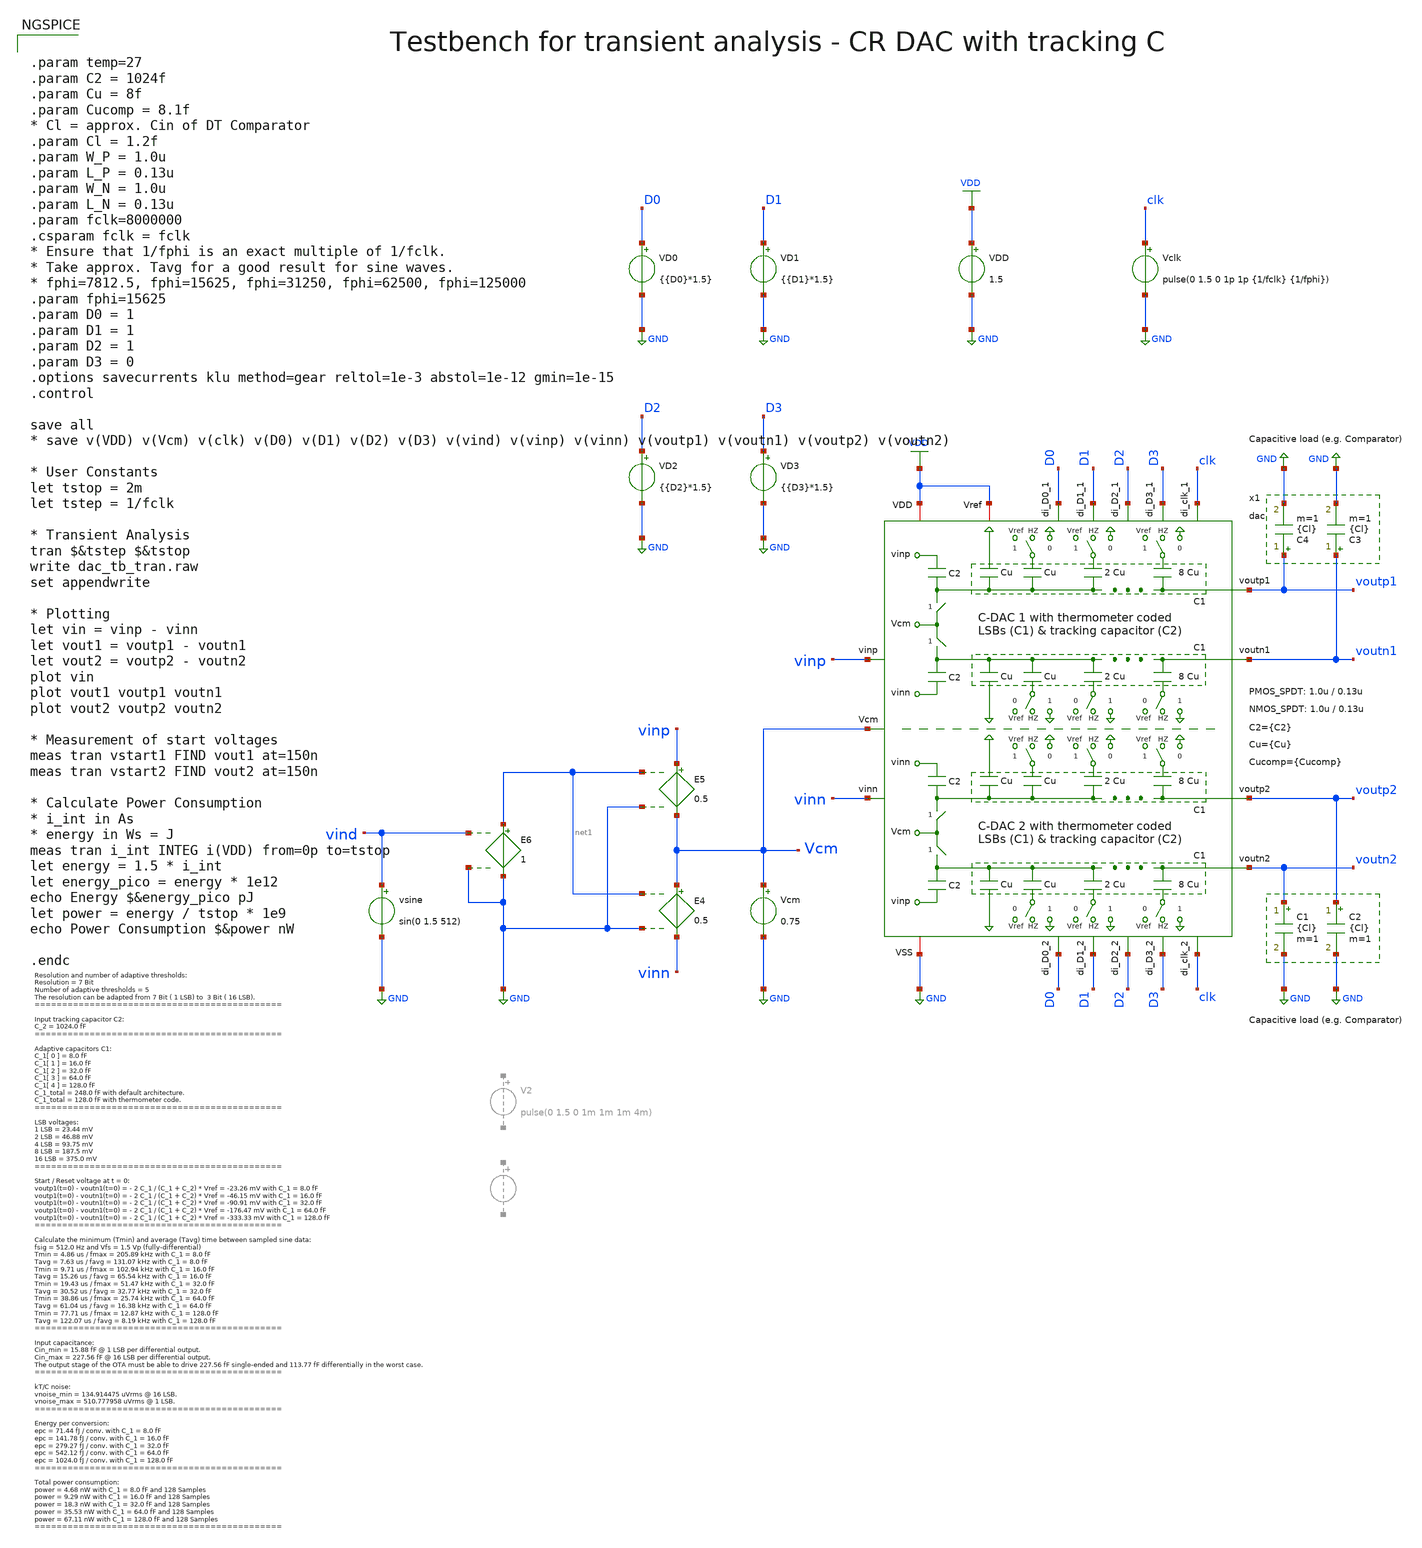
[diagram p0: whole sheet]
** sch_path: SG13G2_ATBS-ADC-main/xschem/dac/testbenches/dac_tb_tran.sch
**.subckt dac_tb_tran
VDD VDD GND 1.5
Vclk clk GND pulse(0 1.5 0 1p 1p {1/fclk} {1/fphi})
Vcm Vcm GND 0.75
E4 Vcm vinn net1 GND 0.5
E5 vinp Vcm net1 GND 0.5
E6 net1 GND vind GND 1
vsine vind GND sin(0 1.5 512)
VD0 D0 GND {{D0}*1.5}
VD1 D1 GND {{D1}*1.5}
VD2 D2 GND {{D2}*1.5}
VD3 D3 GND {{D3}*1.5}
C1 voutn2 GND {Cl} m=1
C2 voutp2 GND {Cl} m=1
C3 voutn1 GND {Cl} m=1
C4 voutp1 GND {Cl} m=1
x1 VDD vinp voutp1 voutn1 vinn D0 D1 D2 D3 GND VDD Vcm voutp2 voutn2 clk D0 D1 D2 D3 clk dac W_P_SPDT=1.0u
+ L_P_SPDT=0.13u W_N_SPDT=1.0u L_N_SPDT=0.13u C2={C2} Cu={Cu} Cucomp={Cucomp}
**** begin user architecture code

.lib cornerMOSlv.lib mos_tt
.lib cornerMOShv.lib mos_tt
.lib cornerRES.lib res_typ



.param temp=27
.param C2 = 1024f
.param Cu = 8f
.param Cucomp = 8.1f
* Cl = approx. Cin of DT Comparator
.param Cl = 1.2f
.param W_P = 1.0u
.param L_P = 0.13u
.param W_N = 1.0u
.param L_N = 0.13u
.param fclk=8000000
.csparam fclk = fclk
* Ensure that 1/fphi is an exact multiple of 1/fclk.
* Take approx. Tavg for a good result for sine waves.
* fphi=7812.5, fphi=15625, fphi=31250, fphi=62500, fphi=125000
.param fphi=15625
.param D0 = 1
.param D1 = 1
.param D2 = 1
.param D3 = 0
.options savecurrents klu method=gear reltol=1e-3 abstol=1e-12 gmin=1e-15
.control

save all
* save v(VDD) v(Vcm) v(clk) v(D0) v(D1) v(D2) v(D3) v(vind) v(vinp) v(vinn) v(voutp1) v(voutn1)
*+ v(voutp2) v(voutn2)

* User Constants
let tstop = 2m
let tstep = 1/fclk

* Transient Analysis
tran $&tstep $&tstop
write dac_tb_tran.raw
set appendwrite

* Plotting
let vin = vinp - vinn
let vout1 = voutp1 - voutn1
let vout2 = voutp2 - voutn2
plot vin
plot vout1 voutp1 voutn1
plot vout2 voutp2 voutn2

* Measurement of start voltages
meas tran vstart1 FIND vout1 at=150n
meas tran vstart2 FIND vout2 at=150n

* Calculate Power Consumption
* i_int in As
* energy in Ws = J
meas tran i_int INTEG i(VDD) from=0p to=tstop
let energy = 1.5 * i_int
let energy_pico = energy * 1e12
echo Energy $&energy_pico pJ
let power = energy / tstop * 1e9
echo Power Consumption $&power nW

.endc


**** end user architecture code
**.ends

* expanding   symbol:  dac/dac.sym # of pins=20
** sym_path: SG13G2_ATBS-ADC-main/xschem/dac/dac.sym
** sch_path: SG13G2_ATBS-ADC-main/xschem/dac/dac.sch
.subckt dac VDD vinp voutp1 voutn1 vinn di_D0_2 di_D1_2 di_D2_2 di_D3_2 VSS Vref Vcm voutp2 voutn2
+ di_clk_2 di_D0_1 di_D1_1 di_D2_1 di_D3_1 di_clk_1  W_P_SPDT=1.0u L_P_SPDT=0.13u W_N_SPDT=1.0u L_N_SPDT=0.13u
+ C2=1024f Cu=8f Cucomp=8.1f
*.opin voutp1
*.ipin di_D0_1
*.iopin VSS
*.iopin Vref
*.opin voutn1
*.ipin vinp
*.ipin vinn
*.ipin di_D1_1
*.ipin di_D2_1
*.ipin di_D3_1
*.opin voutp2
*.opin voutn2
*.iopin VDD
*.ipin Vcm
*.ipin di_clk_1
*.ipin di_D3_2
*.ipin di_D2_2
*.ipin di_D1_2
*.ipin di_D0_2
*.ipin di_clk_2
C2a vinp voutp1 C2 m=1
C2b vinn voutn1 C2 m=1
C1a net3 voutp1 Cucomp m=1
C1b net1 voutn1 Cucomp m=1
x2 VDD di_clk_1 VSS voutp1 Vcm clk_1_n transmission_gate_lv_wo_dummy W_P=1.0u L_P=0.13u W_N=1.0u
+ L_N=0.13u
x3 VDD di_clk_1 VSS voutn1 Vcm clk_1_n transmission_gate_lv_wo_dummy W_P=1.0u L_P=0.13u W_N=1.0u
+ L_N=0.13u
x1 VDD di_clk_1 clk_1_n VSS inverter_lv W_P=W_P_SPDT L_P=L_P_SPDT W_N=W_N_SPDT L_N=L_N_SPDT
x5 Vref VSS VSS di_D1_1 di_clk_1 VDD voutp1 unit_cell W_P_SPDT=W_P_SPDT L_P_SPDT=L_P_SPDT
+ W_N_SPDT=W_N_SPDT L_N_SPDT=L_N_SPDT Cu=2*Cu
x6 Vref VSS VSS di_D2_1 di_clk_1 VDD voutp1 unit_cell W_P_SPDT=W_P_SPDT L_P_SPDT=L_P_SPDT
+ W_N_SPDT=W_N_SPDT L_N_SPDT=L_N_SPDT Cu=4*Cu
x4 Vref VSS VSS di_D0_1 di_clk_1 VDD voutp1 unit_cell W_P_SPDT=W_P_SPDT L_P_SPDT=L_P_SPDT
+ W_N_SPDT=W_N_SPDT L_N_SPDT=L_N_SPDT Cu=Cu
x7 Vref VSS VSS di_D3_1 di_clk_1 VDD voutp1 unit_cell W_P_SPDT=W_P_SPDT L_P_SPDT=L_P_SPDT
+ W_N_SPDT=W_N_SPDT L_N_SPDT=L_N_SPDT Cu=8*Cu
x9 VSS Vref VSS di_D0_1 di_clk_1 VDD voutn1 unit_cell W_P_SPDT=W_P_SPDT L_P_SPDT=L_P_SPDT
+ W_N_SPDT=W_N_SPDT L_N_SPDT=L_N_SPDT Cu=Cu
x10 VSS Vref VSS di_D1_1 di_clk_1 VDD voutn1 unit_cell W_P_SPDT=W_P_SPDT L_P_SPDT=L_P_SPDT
+ W_N_SPDT=W_N_SPDT L_N_SPDT=L_N_SPDT Cu=2*Cu
x11 VSS Vref VSS di_D2_1 di_clk_1 VDD voutn1 unit_cell W_P_SPDT=W_P_SPDT L_P_SPDT=L_P_SPDT
+ W_N_SPDT=W_N_SPDT L_N_SPDT=L_N_SPDT Cu=4*Cu
x12 VSS Vref VSS di_D3_1 di_clk_1 VDD voutn1 unit_cell W_P_SPDT=W_P_SPDT L_P_SPDT=L_P_SPDT
+ W_N_SPDT=W_N_SPDT L_N_SPDT=L_N_SPDT Cu=8*Cu
C1 vinn voutp2 C2 m=1
C2 vinp voutn2 C2 m=1
C1c net2 voutp2 Cucomp m=1
C1d net4 voutn2 Cucomp m=1
x14 VDD di_clk_2 VSS voutp2 Vcm clk_2_n transmission_gate_lv_wo_dummy W_P=1.0u L_P=0.13u W_N=1.0u
+ L_N=0.13u
x15 VDD di_clk_2 VSS voutn2 Vcm clk_2_n transmission_gate_lv_wo_dummy W_P=1.0u L_P=0.13u W_N=1.0u
+ L_N=0.13u
x17 Vref VSS VSS di_D1_2 di_clk_2 VDD voutp2 unit_cell W_P_SPDT=W_P_SPDT L_P_SPDT=L_P_SPDT
+ W_N_SPDT=W_N_SPDT L_N_SPDT=L_N_SPDT Cu=2*Cu
x18 Vref VSS VSS di_D2_2 di_clk_2 VDD voutp2 unit_cell W_P_SPDT=W_P_SPDT L_P_SPDT=L_P_SPDT
+ W_N_SPDT=W_N_SPDT L_N_SPDT=L_N_SPDT Cu=4*Cu
x16 Vref VSS VSS di_D0_2 di_clk_2 VDD voutp2 unit_cell W_P_SPDT=W_P_SPDT L_P_SPDT=L_P_SPDT
+ W_N_SPDT=W_N_SPDT L_N_SPDT=L_N_SPDT Cu=Cu
x19 Vref VSS VSS di_D3_2 di_clk_2 VDD voutp2 unit_cell W_P_SPDT=W_P_SPDT L_P_SPDT=L_P_SPDT
+ W_N_SPDT=W_N_SPDT L_N_SPDT=L_N_SPDT Cu=8*Cu
x21 VSS Vref VSS di_D0_2 di_clk_2 VDD voutn2 unit_cell W_P_SPDT=W_P_SPDT L_P_SPDT=L_P_SPDT
+ W_N_SPDT=W_N_SPDT L_N_SPDT=L_N_SPDT Cu=Cu
x22 VSS Vref VSS di_D1_2 di_clk_2 VDD voutn2 unit_cell W_P_SPDT=W_P_SPDT L_P_SPDT=L_P_SPDT
+ W_N_SPDT=W_N_SPDT L_N_SPDT=L_N_SPDT Cu=2*Cu
x23 VSS Vref VSS di_D2_2 di_clk_2 VDD voutn2 unit_cell W_P_SPDT=W_P_SPDT L_P_SPDT=L_P_SPDT
+ W_N_SPDT=W_N_SPDT L_N_SPDT=L_N_SPDT Cu=4*Cu
x24 VSS Vref VSS di_D3_2 di_clk_2 VDD voutn2 unit_cell W_P_SPDT=W_P_SPDT L_P_SPDT=L_P_SPDT
+ W_N_SPDT=W_N_SPDT L_N_SPDT=L_N_SPDT Cu=8*Cu
x8 VDD di_clk_1 VSS net3 VSS Vref spdt_switch W_P_TG=W_P_SPDT L_P_TG=L_P_SPDT W_N_TG=W_N_SPDT
+ L_N_TG=L_N_SPDT
x13 VDD di_clk_1 VSS net1 Vref VSS spdt_switch W_P_TG=W_P_SPDT L_P_TG=L_P_SPDT W_N_TG=W_N_SPDT
+ L_N_TG=L_N_SPDT
x20 VDD di_clk_2 VSS net2 VSS Vref spdt_switch W_P_TG=W_P_SPDT L_P_TG=L_P_SPDT W_N_TG=W_N_SPDT
+ L_N_TG=L_N_SPDT
x25 VDD di_clk_2 VSS net4 Vref VSS spdt_switch W_P_TG=W_P_SPDT L_P_TG=L_P_SPDT W_N_TG=W_N_SPDT
+ L_N_TG=L_N_SPDT
x26 VDD di_clk_2 clk_2_n VSS inverter_lv W_P=W_P_SPDT L_P=L_P_SPDT W_N=W_N_SPDT L_N=L_N_SPDT
.ends


* expanding   symbol:  transmission_gate/transmission_gate_lv_wo_dummy.sym # of pins=6
** sym_path: SG13G2_ATBS-ADC-main/xschem/transmission_gate/transmission_gate_lv_wo_dummy.sym
** sch_path: SG13G2_ATBS-ADC-main/xschem/transmission_gate/transmission_gate_lv_wo_dummy.sch
.subckt transmission_gate_lv_wo_dummy VDD di_tg_ctrl VSS v_b v_a di_tg_ctrl_n  W_P=1.0u L_P=0.13u
+ W_N=1.0u L_N=0.13u
*.iopin v_a
*.iopin v_b
*.iopin VDD
*.iopin VSS
*.ipin di_tg_ctrl
*.ipin di_tg_ctrl_n
XM1 v_a di_tg_ctrl v_b VSS sg13_lv_nmos w=W_N l=L_N ng=1 m=1 mm_ok=1
XM2 v_a di_tg_ctrl_n v_b VDD sg13_lv_pmos w=W_P l=L_P ng=1 m=1 mm_ok=1
.ends


* expanding   symbol:  inverter/inverter_lv.sym # of pins=4
** sym_path: SG13G2_ATBS-ADC-main/xschem/inverter/inverter_lv.sym
** sch_path: SG13G2_ATBS-ADC-main/xschem/inverter/inverter_lv.sch
.subckt inverter_lv VDD vin vout VSS  W_P=3.0u L_P=0.13u W_N=1.0u L_N=0.13u
*.ipin vin
*.iopin VDD
*.iopin VSS
*.opin vout
XM1 vout vin VDD VDD sg13_lv_pmos w=W_P l=L_P ng=1 m=1 mm_ok=1
XM2 vout vin VSS VSS sg13_lv_nmos w=W_N l=L_N ng=1 m=1 mm_ok=1
.ends


* expanding   symbol:  dac/unit_cell.sym # of pins=7
** sym_path: SG13G2_ATBS-ADC-main/xschem/dac/unit_cell.sym
** sch_path: SG13G2_ATBS-ADC-main/xschem/dac/unit_cell.sch
.subckt unit_cell v1 v0 VSS di_cell_en di_clk VDD vtop  W_P_SPDT=1.0u L_P_SPDT=0.13u W_N_SPDT=1.0u
+ L_N_SPDT=0.13u Cu=8f
*.ipin di_cell_en
*.iopin VSS
*.iopin v0
*.iopin VDD
*.ipin di_clk
*.iopin v1
*.iopin vtop
x1 VDD di_clk VSS net1 v0 v1 di_cell_en_n spdt_hz_switch W_P_TG=W_P_SPDT L_P_TG=L_P_SPDT
+ W_N_TG=W_N_SPDT L_N_TG=L_N_SPDT
C1 net1 vtop Cu m=1
x3 VDD di_cell_en di_cell_en_n VSS inverter_lv W_P=W_P_SPDT L_P=W_P_SPDT W_N=W_N_SPDT L_N=W_N_SPDT
.ends


* expanding   symbol:  spdt_switch/spdt_switch.sym # of pins=6
** sym_path: SG13G2_ATBS-ADC-main/xschem/spdt_switch/spdt_switch.sym
** sch_path: SG13G2_ATBS-ADC-main/xschem/spdt_switch/spdt_switch.sch
.subckt spdt_switch VDD di_spdt_ctrl VSS v_c v_b v_a  W_P_TG=3.0u L_P_TG=0.13u W_N_TG=1.0u
+ L_N_TG=0.13u
*.iopin v_a
*.iopin v_b
*.iopin v_c
*.iopin VDD
*.iopin VSS
*.ipin di_spdt_ctrl
x1 VDD di_spdt_ctrl VSS v_c v_a di_spdt_ctrl_n transmission_gate_lv_wo_dummy W_P=W_P_TG L_P=L_P_TG
+ W_N=W_N_TG L_N=L_N_TG
x2 VDD di_spdt_ctrl_n VSS v_b v_c di_spdt_ctrl transmission_gate_lv_wo_dummy W_P=W_P_TG L_P=L_P_TG
+ W_N=W_N_TG L_N=L_N_TG
x8 VDD di_spdt_ctrl di_spdt_ctrl_n VSS inverter_lv W_P=W_P_TG L_P=L_P_TG W_N=W_N_TG L_N=L_N_TG
.ends


* expanding   symbol:  spdt_switch/spdt_hz_switch.sym # of pins=7
** sym_path: SG13G2_ATBS-ADC-main/xschem/spdt_switch/spdt_hz_switch.sym
** sch_path: SG13G2_ATBS-ADC-main/xschem/spdt_switch/spdt_hz_switch.sch
.subckt spdt_hz_switch VDD di_spdt_ctrl VSS v_c v_b v_a di_spdt_hz  W_P_TG=3.0u L_P_TG=0.13u
+ W_N_TG=1.0u L_N_TG=0.13u
*.iopin v_a
*.iopin v_b
*.iopin v_c
*.iopin VDD
*.iopin VSS
*.ipin di_spdt_ctrl
*.ipin di_spdt_hz
x1 VDD di_spdt_ctrl VSS net1 v_a di_spdt_ctrl_n transmission_gate_lv_wo_dummy W_P=W_P_TG L_P=L_P_TG
+ W_N=W_N_TG L_N=L_N_TG
x2 VDD di_spdt_ctrl_n VSS v_b net1 di_spdt_ctrl transmission_gate_lv_wo_dummy W_P=W_P_TG L_P=L_P_TG
+ W_N=W_N_TG L_N=L_N_TG
x8 VDD di_spdt_ctrl di_spdt_ctrl_n VSS inverter_lv W_P=W_P_TG L_P=L_P_TG W_N=W_N_TG L_N=L_N_TG
x3 VDD di_spdt_hz di_spdt_hz_n VSS inverter_lv W_P=W_P_TG L_P=L_P_TG W_N=W_N_TG L_N=L_N_TG
x4 VDD di_spdt_hz_n VSS v_c net1 di_spdt_hz transmission_gate_lv_wo_dummy W_P=W_P_TG L_P=L_P_TG
+ W_N=W_N_TG L_N=L_N_TG
.ends

.GLOBAL GND
.GLOBAL VDD
.end
